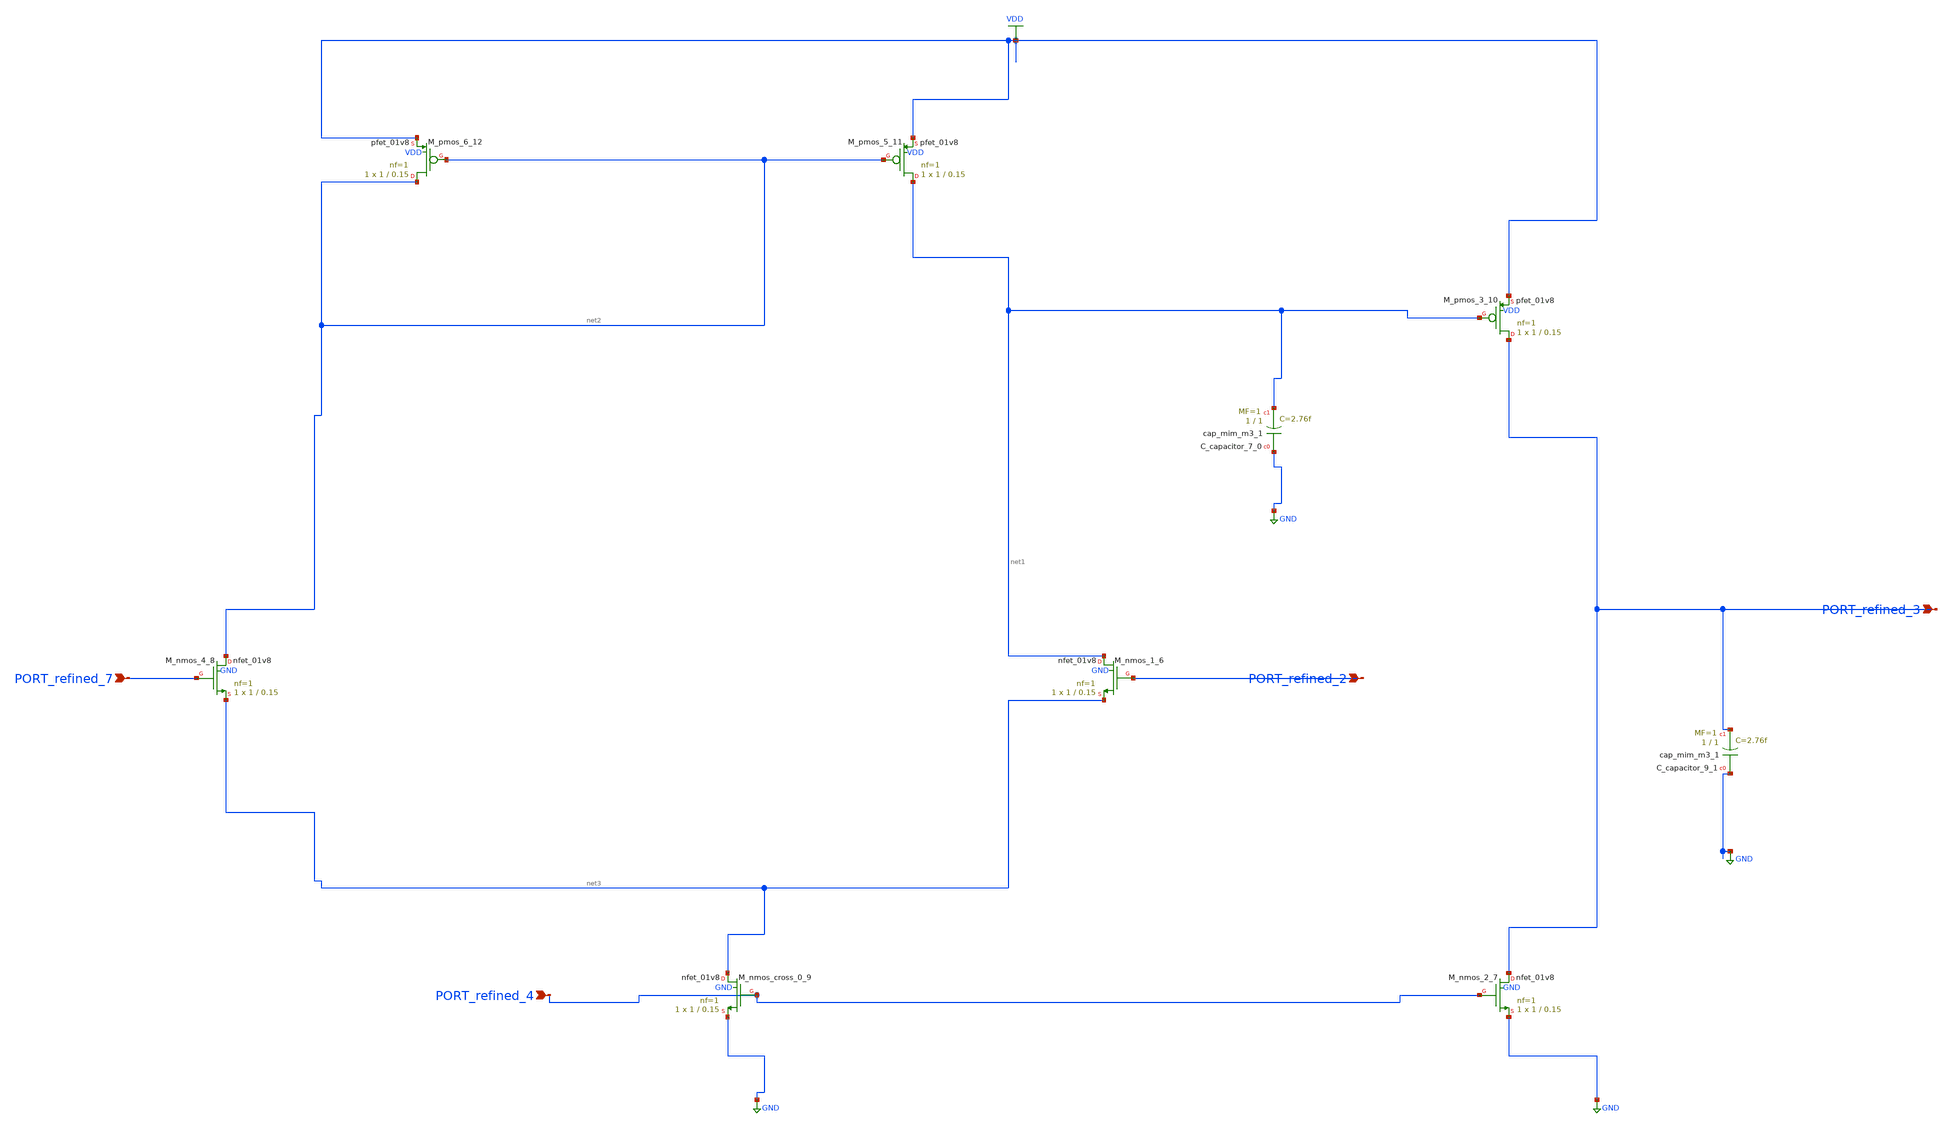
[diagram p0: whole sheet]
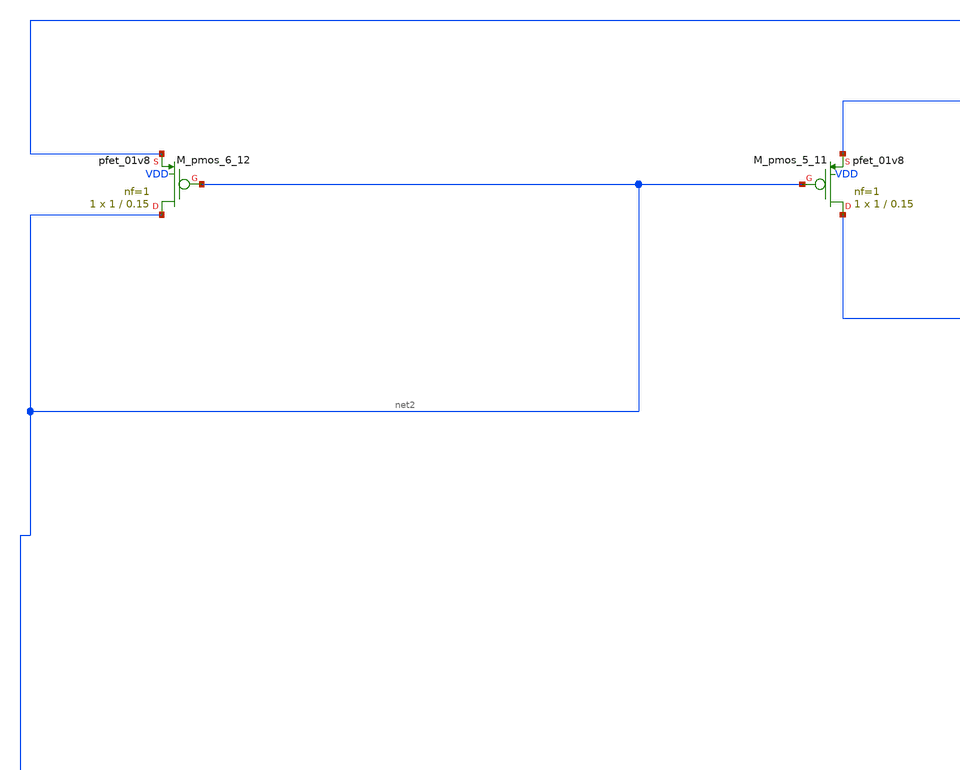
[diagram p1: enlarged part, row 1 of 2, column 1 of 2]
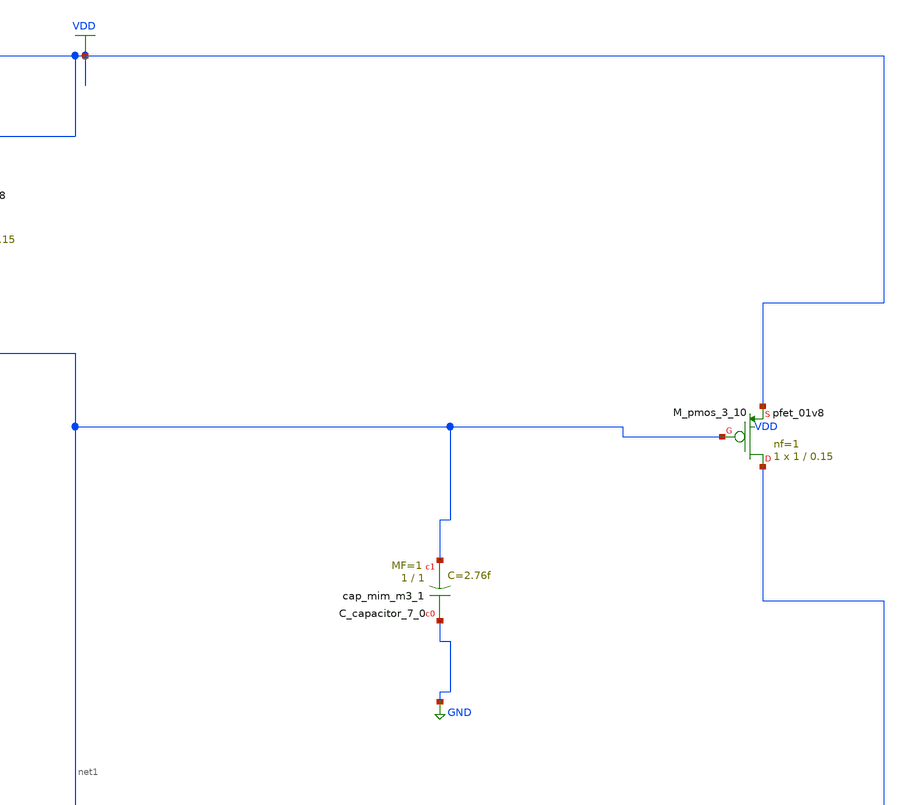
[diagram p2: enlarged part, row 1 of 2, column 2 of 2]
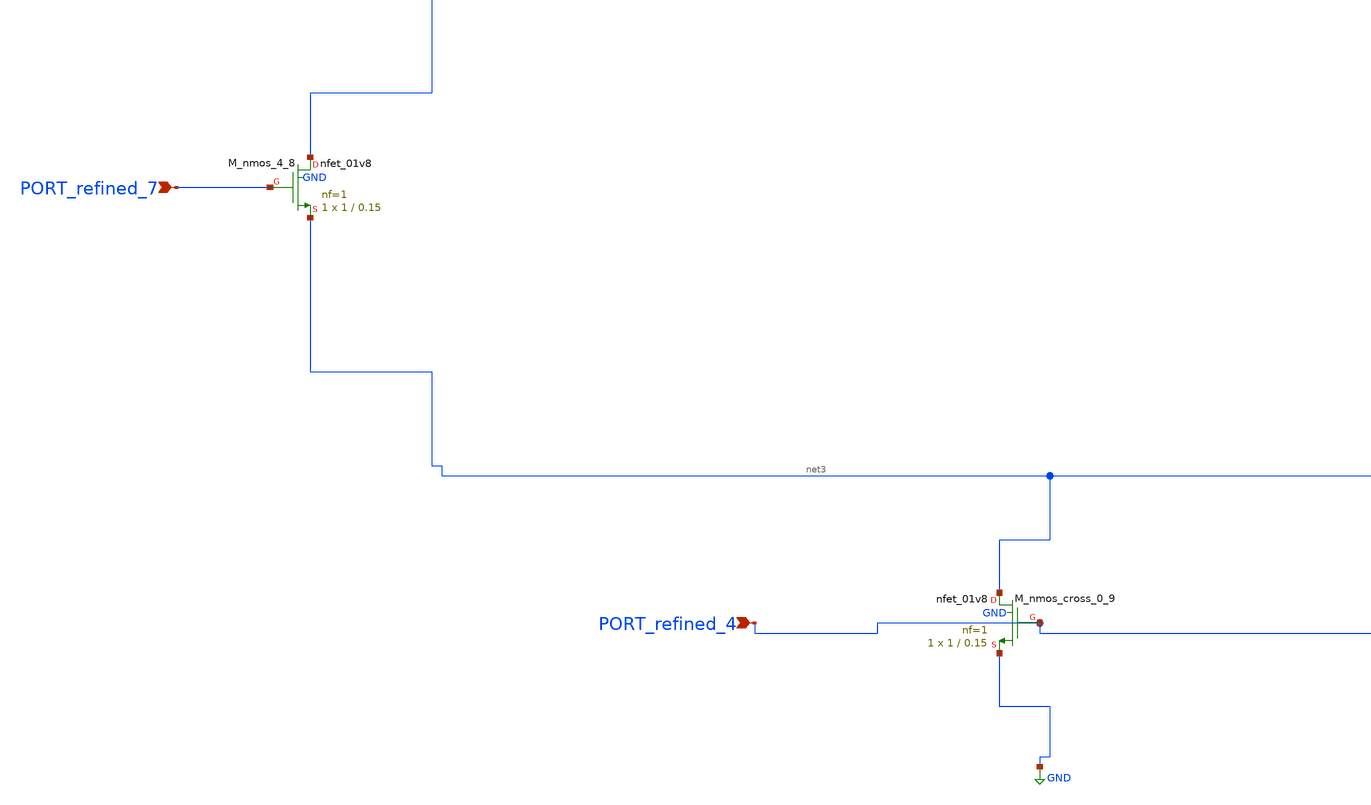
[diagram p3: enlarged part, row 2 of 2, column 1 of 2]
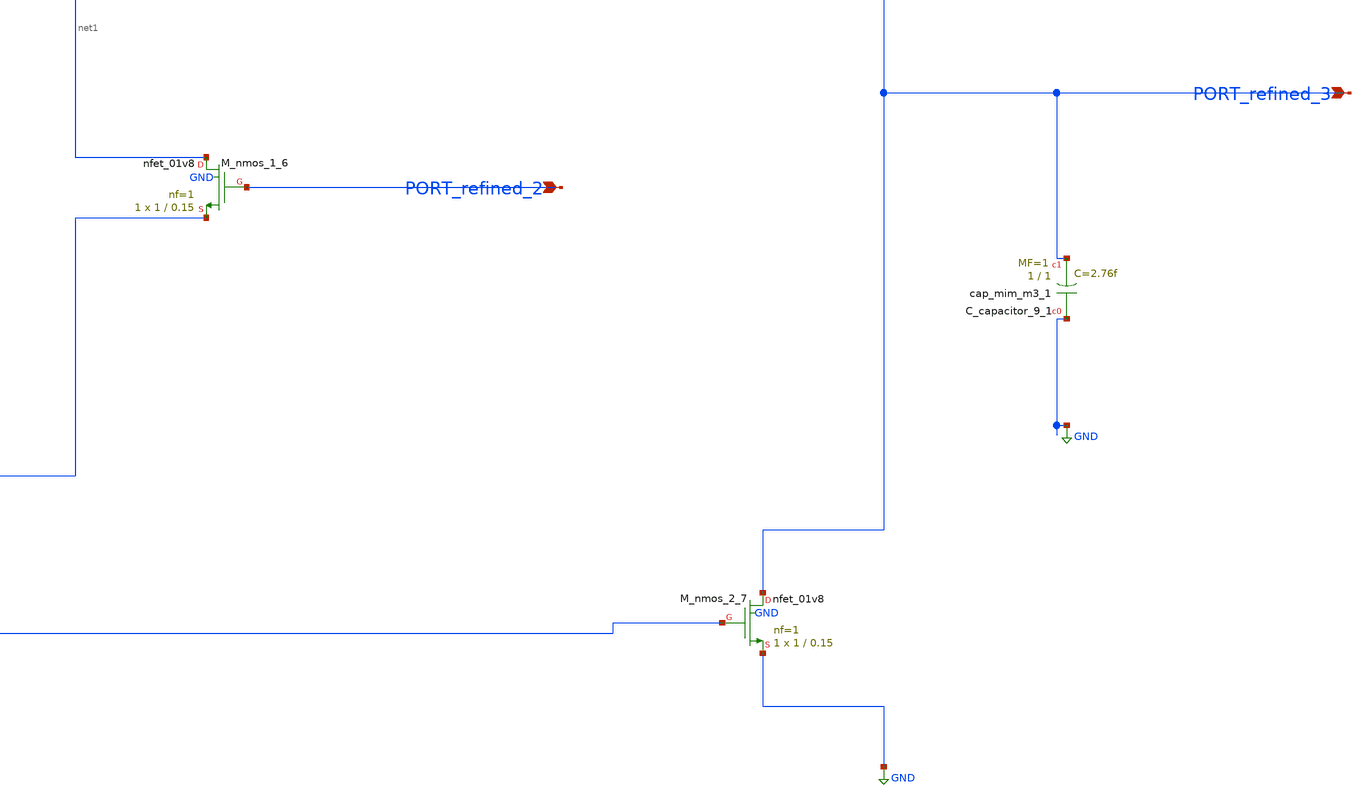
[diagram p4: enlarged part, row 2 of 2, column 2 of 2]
** sch_path: schematics/Image2Net/122.sch
**.subckt 122 PORT_refined_4 PORT_refined_7 PORT_refined_3 PORT_refined_2
*.ipin PORT_refined_4
*.ipin PORT_refined_7
*.ipin PORT_refined_3
*.ipin PORT_refined_2
XC_capacitor_7_0 GND net1 sky130_fd_pr__cap_mim_m3_1 W=1 L=1 MF=1 m=1
XC_capacitor_9_1 GND PORT_refined_3 sky130_fd_pr__cap_mim_m3_1 W=1 L=1 MF=1 m=1
XM_nmos_1_6 net1 PORT_refined_2 net3 GND sky130_fd_pr__nfet_01v8 L=0.15 W=1 nf=1 ad='int((1 + 1)/2) * 1 / 1 * 0.29'
+ as='int((1 + 2)/2) * 1 / 1 * 0.29' pd='2*int((1 + 1)/2) * (1 / 1 + 0.29)' ps='2*int((1 + 2)/2) * (1 / 1 + 0.29)'
+ nrd='0.29 / 1 ' nrs='0.29 / 1 ' sa=0 sb=0 sd=0 mult=1 m=1
XM_nmos_2_7 PORT_refined_3 PORT_refined_4 GND GND sky130_fd_pr__nfet_01v8 L=0.15 W=1 nf=1 ad='int((1 + 1)/2) * 1 / 1 * 0.29'
+ as='int((1 + 2)/2) * 1 / 1 * 0.29' pd='2*int((1 + 1)/2) * (1 / 1 + 0.29)' ps='2*int((1 + 2)/2) * (1 / 1 + 0.29)'
+ nrd='0.29 / 1 ' nrs='0.29 / 1 ' sa=0 sb=0 sd=0 mult=1 m=1
XM_nmos_4_8 net2 PORT_refined_7 net3 GND sky130_fd_pr__nfet_01v8 L=0.15 W=1 nf=1 ad='int((1 + 1)/2) * 1 / 1 * 0.29'
+ as='int((1 + 2)/2) * 1 / 1 * 0.29' pd='2*int((1 + 1)/2) * (1 / 1 + 0.29)' ps='2*int((1 + 2)/2) * (1 / 1 + 0.29)'
+ nrd='0.29 / 1 ' nrs='0.29 / 1 ' sa=0 sb=0 sd=0 mult=1 m=1
XM_nmos_cross_0_9 net3 PORT_refined_4 GND GND sky130_fd_pr__nfet_01v8 L=0.15 W=1 nf=1 ad='int((1 + 1)/2) * 1 / 1 * 0.29'
+ as='int((1 + 2)/2) * 1 / 1 * 0.29' pd='2*int((1 + 1)/2) * (1 / 1 + 0.29)' ps='2*int((1 + 2)/2) * (1 / 1 + 0.29)'
+ nrd='0.29 / 1 ' nrs='0.29 / 1 ' sa=0 sb=0 sd=0 mult=1 m=1
XM_pmos_3_10 PORT_refined_3 net1 VDD VDD sky130_fd_pr__pfet_01v8 L=0.15 W=1 nf=1 ad='int((1 + 1)/2) * 1 / 1 * 0.29'
+ as='int((1 + 2)/2) * 1 / 1 * 0.29' pd='2*int((1 + 1)/2) * (1 / 1 + 0.29)' ps='2*int((1 + 2)/2) * (1 / 1 + 0.29)'
+ nrd='0.29 / 1 ' nrs='0.29 / 1 ' sa=0 sb=0 sd=0 mult=1 m=1
XM_pmos_5_11 net1 net2 VDD VDD sky130_fd_pr__pfet_01v8 L=0.15 W=1 nf=1 ad='int((1 + 1)/2) * 1 / 1 * 0.29'
+ as='int((1 + 2)/2) * 1 / 1 * 0.29' pd='2*int((1 + 1)/2) * (1 / 1 + 0.29)' ps='2*int((1 + 2)/2) * (1 / 1 + 0.29)'
+ nrd='0.29 / 1 ' nrs='0.29 / 1 ' sa=0 sb=0 sd=0 mult=1 m=1
XM_pmos_6_12 net2 net2 VDD VDD sky130_fd_pr__pfet_01v8 L=0.15 W=1 nf=1 ad='int((1 + 1)/2) * 1 / 1 * 0.29'
+ as='int((1 + 2)/2) * 1 / 1 * 0.29' pd='2*int((1 + 1)/2) * (1 / 1 + 0.29)' ps='2*int((1 + 2)/2) * (1 / 1 + 0.29)'
+ nrd='0.29 / 1 ' nrs='0.29 / 1 ' sa=0 sb=0 sd=0 mult=1 m=1
**.ends
.GLOBAL GND
.GLOBAL VDD
.end
